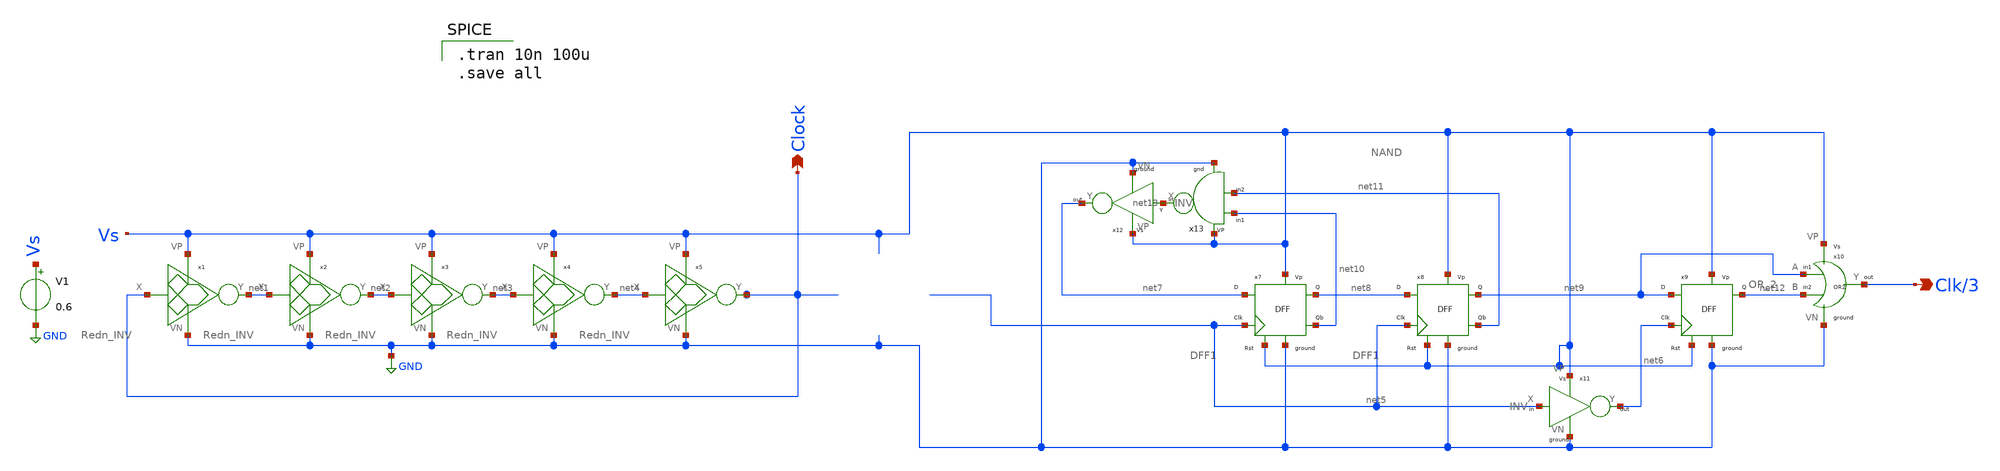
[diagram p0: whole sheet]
** sch_path: Blocks/Clk_generator/RingOsci_Div3.sch
**.subckt RingOsci_Div3 Clock Clk/3
*.opin Clock
*.opin Clk/3
V1 Vs GND 0.6
x7 net7 net5 Vs GND Vs net8 net10 DFF1
x8 net8 net5 Vs GND Vs net9 net11 DFF1
x9 net9 net6 Vs GND Vs net12 DFF
x10 net12 net9 Clk/3 Vs GND OR_2
x11 net5 net6 Vs GND INV
x12 net13 net7 Vs GND INV
x13 net11 net10 net13 Vs GND NAND
x1 Clock net1 Vs GND Redn_INV
x2 net1 net2 Vs GND Redn_INV
x3 net2 net3 Vs GND Redn_INV
x4 net3 net4 Vs GND Redn_INV
x5 net4 Clock Vs GND Redn_INV
**** begin user architecture code

.tran 10n 100u
.save all


** opencircuitdesign pdks install
.lib $::SKYWATER_MODELS/sky130.lib.spice tt


**** end user architecture code
**.ends

* expanding   symbol:  Pico_project/FlipFlops/DFF1.sym # of pins=7
** sym_path: component/FlipFlops/DFF1.sym
** sch_path: component/FlipFlops/DFF1.sch
.subckt DFF1 D Clk RST VN VP Q Qb
*.opin Q
*.iopin VN
*.iopin VP
*.ipin Clk
*.ipin D
*.ipin RST
*.opin Qb
x7 net2 net4 net3 VP VN NAND
x8 net3 Clk RST VP VN net2 NAND3
x6 Q net1 RST VP VN Qb NAND3
x4 net2 Clk net4 VP VN net1 NAND3
x5 net1 D RST VP VN net4 NAND3
x1 Qb net2 Q VP VN NAND
.ends


* expanding   symbol:  Pico_project/FlipFlops/DFF.sym # of pins=6
** sym_path: component/FlipFlops/DFF.sym
** sch_path: component/FlipFlops/DFF.sch
.subckt DFF D Clk RST VN VP Q
*.opin Q
*.iopin VN
*.iopin VP
*.ipin Clk
*.ipin D
*.ipin RST
x1 net2 net5 net4 VP VN NAND
x7 net4 Clk RST VP VN net2 NAND3
x3 Q net1 RST VP VN net3 NAND3
x4 net2 Clk net5 VP VN net1 NAND3
x5 net1 D RST VP VN net5 NAND3
x6 net3 net2 Q VP VN NAND
.ends


* expanding   symbol:  Pico_project/OR2/OR_2.sym # of pins=5
** sym_path: component/OR2/OR_2.sym
** sch_path: component/OR2/OR_2.sch
.subckt OR_2 B A Y VP VN
*.iopin VP
*.iopin VN
*.ipin A
*.ipin B
*.opin Y
XM1 net1 B VN VN sky130_fd_pr__nfet_01v8 L=0.15 W=0.42 nf=1 ad='int((nf+1)/2) * W/nf * 0.29' as='int((nf+2)/2) * W/nf * 0.29'
+ pd='2*int((nf+1)/2) * (W/nf + 0.29)' ps='2*int((nf+2)/2) * (W/nf + 0.29)' nrd='0.29 / W' nrs='0.29 / W'
+ sa=0 sb=0 sd=0 mult=1 m=1
XM2 net1 A VN VN sky130_fd_pr__nfet_01v8 L=0.15 W=0.42 nf=1 ad='int((nf+1)/2) * W/nf * 0.29' as='int((nf+2)/2) * W/nf * 0.29'
+ pd='2*int((nf+1)/2) * (W/nf + 0.29)' ps='2*int((nf+2)/2) * (W/nf + 0.29)' nrd='0.29 / W' nrs='0.29 / W'
+ sa=0 sb=0 sd=0 mult=1 m=1
XM3 net1 B net2 VP sky130_fd_pr__pfet_01v8 L=0.15 W=2.52 nf=1 ad='int((nf+1)/2) * W/nf * 0.29' as='int((nf+2)/2) * W/nf * 0.29'
+ pd='2*int((nf+1)/2) * (W/nf + 0.29)' ps='2*int((nf+2)/2) * (W/nf + 0.29)' nrd='0.29 / W' nrs='0.29 / W'
+ sa=0 sb=0 sd=0 mult=1 m=1
XM4 net2 A VP VP sky130_fd_pr__pfet_01v8 L=0.15 W=2.52 nf=1 ad='int((nf+1)/2) * W/nf * 0.29' as='int((nf+2)/2) * W/nf * 0.29'
+ pd='2*int((nf+1)/2) * (W/nf + 0.29)' ps='2*int((nf+2)/2) * (W/nf + 0.29)' nrd='0.29 / W' nrs='0.29 / W'
+ sa=0 sb=0 sd=0 mult=1 m=1
x1 net1 Y VP VN INV
.ends


* expanding   symbol:  Pico_project/INV/INV.sym # of pins=4
** sym_path: component/INV/INV.sym
** sch_path: component/INV/INV.sch
.subckt INV X Y VP VN
*.ipin X
*.opin Y
*.iopin VN
*.iopin VP
XM1 Y X VN VN sky130_fd_pr__nfet_01v8 L=0.15 W=0.42 nf=1 ad='int((nf+1)/2) * W/nf * 0.29' as='int((nf+2)/2) * W/nf * 0.29'
+ pd='2*int((nf+1)/2) * (W/nf + 0.29)' ps='2*int((nf+2)/2) * (W/nf + 0.29)' nrd='0.29 / W' nrs='0.29 / W'
+ sa=0 sb=0 sd=0 mult=1 m=1
XM2 Y X VP VP sky130_fd_pr__pfet_01v8 L=0.15 W=1.26 nf=1 ad='int((nf+1)/2) * W/nf * 0.29' as='int((nf+2)/2) * W/nf * 0.29'
+ pd='2*int((nf+1)/2) * (W/nf + 0.29)' ps='2*int((nf+2)/2) * (W/nf + 0.29)' nrd='0.29 / W' nrs='0.29 / W'
+ sa=0 sb=0 sd=0 mult=1 m=1
.ends


* expanding   symbol:  Pico_project/NAND2/NAND.sym # of pins=5
** sym_path: component/NAND2/NAND.sym
** sch_path: component/NAND2/NAND.sch
.subckt NAND B A Y VP VN
*.iopin VP
*.ipin A
*.ipin B
*.opin Y
*.iopin VN
XM1 Y A VP VP sky130_fd_pr__pfet_01v8 L=0.15 W=1.26 nf=1 ad='int((nf+1)/2) * W/nf * 0.29' as='int((nf+2)/2) * W/nf * 0.29'
+ pd='2*int((nf+1)/2) * (W/nf + 0.29)' ps='2*int((nf+2)/2) * (W/nf + 0.29)' nrd='0.29 / W' nrs='0.29 / W'
+ sa=0 sb=0 sd=0 mult=1 m=1
XM2 Y B VP VP sky130_fd_pr__pfet_01v8 L=0.15 W=1.26 nf=1 ad='int((nf+1)/2) * W/nf * 0.29' as='int((nf+2)/2) * W/nf * 0.29'
+ pd='2*int((nf+1)/2) * (W/nf + 0.29)' ps='2*int((nf+2)/2) * (W/nf + 0.29)' nrd='0.29 / W' nrs='0.29 / W'
+ sa=0 sb=0 sd=0 mult=1 m=1
XM3 Y A net1 net1 sky130_fd_pr__nfet_01v8 L=0.15 W=0.84 nf=1 ad='int((nf+1)/2) * W/nf * 0.29' as='int((nf+2)/2) * W/nf * 0.29'
+ pd='2*int((nf+1)/2) * (W/nf + 0.29)' ps='2*int((nf+2)/2) * (W/nf + 0.29)' nrd='0.29 / W' nrs='0.29 / W'
+ sa=0 sb=0 sd=0 mult=1 m=1
XM4 net1 B VN VN sky130_fd_pr__nfet_01v8 L=0.15 W=0.84 nf=1 ad='int((nf+1)/2) * W/nf * 0.29' as='int((nf+2)/2) * W/nf * 0.29'
+ pd='2*int((nf+1)/2) * (W/nf + 0.29)' ps='2*int((nf+2)/2) * (W/nf + 0.29)' nrd='0.29 / W' nrs='0.29 / W'
+ sa=0 sb=0 sd=0 mult=1 m=1
.ends


* expanding   symbol:  pico/akshat_comp/ezyzip/PICO/project_file/Redn_INV.sym # of pins=4
** sym_path: component/Reduntant_Inverter/Redn_INV.sym
** sch_path: component/Reduntant_Inverter/Redn_INV.sch
.subckt Redn_INV X Y VP VN
*.opin Y
*.ipin X
*.iopin VP
*.iopin VN
XM15 net4 X VN VN sky130_fd_pr__nfet_01v8_lvt L=0.15 W=1 nf=1 ad='int((nf+1)/2) * W/nf * 0.29' as='int((nf+2)/2) * W/nf * 0.29'
+ pd='2*int((nf+1)/2) * (W/nf + 0.29)' ps='2*int((nf+2)/2) * (W/nf + 0.29)' nrd='0.29 / W' nrs='0.29 / W'
+ sa=0 sb=0 sd=0 mult=1 m=1
XM1 net5 X net3 VN sky130_fd_pr__nfet_01v8_lvt L=0.15 W=3.25 nf=1 ad='int((nf+1)/2) * W/nf * 0.29' as='int((nf+2)/2) * W/nf * 0.29'
+ pd='2*int((nf+1)/2) * (W/nf + 0.29)' ps='2*int((nf+2)/2) * (W/nf + 0.29)' nrd='0.29 / W' nrs='0.29 / W'
+ sa=0 sb=0 sd=0 mult=1 m=1
XM16 Y X net6 VN sky130_fd_pr__nfet_01v8_lvt L=0.15 W=6.5 nf=1 ad='int((nf+1)/2) * W/nf * 0.29' as='int((nf+2)/2) * W/nf * 0.29'
+ pd='2*int((nf+1)/2) * (W/nf + 0.29)' ps='2*int((nf+2)/2) * (W/nf + 0.29)' nrd='0.29 / W' nrs='0.29 / W'
+ sa=0 sb=0 sd=0 mult=1 m=1
XM17 net3 X VN VN sky130_fd_pr__nfet_01v8_lvt L=0.15 W=3.25 nf=1 ad='int((nf+1)/2) * W/nf * 0.29' as='int((nf+2)/2) * W/nf * 0.29'
+ pd='2*int((nf+1)/2) * (W/nf + 0.29)' ps='2*int((nf+2)/2) * (W/nf + 0.29)' nrd='0.29 / W' nrs='0.29 / W'
+ sa=0 sb=0 sd=0 mult=1 m=1
XM18 net2 X VN VN sky130_fd_pr__nfet_01v8_lvt L=0.15 W=1.5 nf=1 ad='int((nf+1)/2) * W/nf * 0.29' as='int((nf+2)/2) * W/nf * 0.29'
+ pd='2*int((nf+1)/2) * (W/nf + 0.29)' ps='2*int((nf+2)/2) * (W/nf + 0.29)' nrd='0.29 / W' nrs='0.29 / W'
+ sa=0 sb=0 sd=0 mult=1 m=1
XM19 net1 X VN VN sky130_fd_pr__nfet_01v8_lvt L=0.15 W=6.5 nf=1 ad='int((nf+1)/2) * W/nf * 0.29' as='int((nf+2)/2) * W/nf * 0.29'
+ pd='2*int((nf+1)/2) * (W/nf + 0.29)' ps='2*int((nf+2)/2) * (W/nf + 0.29)' nrd='0.29 / W' nrs='0.29 / W'
+ sa=0 sb=0 sd=0 mult=1 m=1
XM20 net6 X net1 VN sky130_fd_pr__nfet_01v8_lvt L=0.15 W=6.5 nf=1 ad='int((nf+1)/2) * W/nf * 0.29' as='int((nf+2)/2) * W/nf * 0.29'
+ pd='2*int((nf+1)/2) * (W/nf + 0.29)' ps='2*int((nf+2)/2) * (W/nf + 0.29)' nrd='0.29 / W' nrs='0.29 / W'
+ sa=0 sb=0 sd=0 mult=1 m=1
XM2 net4 X VP VP sky130_fd_pr__pfet_01v8 L=0.15 W=10 nf=1 ad='int((nf+1)/2) * W/nf * 0.29' as='int((nf+2)/2) * W/nf * 0.29'
+ pd='2*int((nf+1)/2) * (W/nf + 0.29)' ps='2*int((nf+2)/2) * (W/nf + 0.29)' nrd='0.29 / W' nrs='0.29 / W'
+ sa=0 sb=0 sd=0 mult=1 m=1
XM5 net5 X net4 net4 sky130_fd_pr__pfet_01v8 L=0.15 W=10 nf=1 ad='int((nf+1)/2) * W/nf * 0.29' as='int((nf+2)/2) * W/nf * 0.29'
+ pd='2*int((nf+1)/2) * (W/nf + 0.29)' ps='2*int((nf+2)/2) * (W/nf + 0.29)' nrd='0.29 / W' nrs='0.29 / W'
+ sa=0 sb=0 sd=0 mult=1 m=1
XM6 Y X net5 VP sky130_fd_pr__pfet_01v8 L=0.15 W=10 nf=1 ad='int((nf+1)/2) * W/nf * 0.29' as='int((nf+2)/2) * W/nf * 0.29'
+ pd='2*int((nf+1)/2) * (W/nf + 0.29)' ps='2*int((nf+2)/2) * (W/nf + 0.29)' nrd='0.29 / W' nrs='0.29 / W'
+ sa=0 sb=0 sd=0 mult=1 m=1
XM8 net3 X VP VP sky130_fd_pr__pfet_01v8 L=0.15 W=2 nf=1 ad='int((nf+1)/2) * W/nf * 0.29' as='int((nf+2)/2) * W/nf * 0.29'
+ pd='2*int((nf+1)/2) * (W/nf + 0.29)' ps='2*int((nf+2)/2) * (W/nf + 0.29)' nrd='0.29 / W' nrs='0.29 / W'
+ sa=0 sb=0 sd=0 mult=1 m=1
XM12 net2 X VP VP sky130_fd_pr__pfet_01v8 L=0.15 W=5 nf=1 ad='int((nf+1)/2) * W/nf * 0.29' as='int((nf+2)/2) * W/nf * 0.29'
+ pd='2*int((nf+1)/2) * (W/nf + 0.29)' ps='2*int((nf+2)/2) * (W/nf + 0.29)' nrd='0.29 / W' nrs='0.29 / W'
+ sa=0 sb=0 sd=0 mult=1 m=1
XM14 net6 X net2 VP sky130_fd_pr__pfet_01v8 L=0.15 W=5 nf=1 ad='int((nf+1)/2) * W/nf * 0.29' as='int((nf+2)/2) * W/nf * 0.29'
+ pd='2*int((nf+1)/2) * (W/nf + 0.29)' ps='2*int((nf+2)/2) * (W/nf + 0.29)' nrd='0.29 / W' nrs='0.29 / W'
+ sa=0 sb=0 sd=0 mult=1 m=1
XM21 net1 X VP VP sky130_fd_pr__pfet_01v8 L=0.15 W=1.5 nf=1 ad='int((nf+1)/2) * W/nf * 0.29' as='int((nf+2)/2) * W/nf * 0.29'
+ pd='2*int((nf+1)/2) * (W/nf + 0.29)' ps='2*int((nf+2)/2) * (W/nf + 0.29)' nrd='0.29 / W' nrs='0.29 / W'
+ sa=0 sb=0 sd=0 mult=1 m=1
.ends


* expanding   symbol:  component/NAND3/NAND3.sym # of pins=6
** sym_path: component/NAND3/NAND3.sym
** sch_path: component/NAND3/NAND3.sch
.subckt NAND3 A B C VP VN Y
*.iopin VP
*.iopin VN
*.ipin A
*.ipin B
*.ipin C
*.opin Y
XM1 Y A net1 VN sky130_fd_pr__nfet_01v8 L=0.15 W=1.26 nf=1 ad='int((nf+1)/2) * W/nf * 0.29' as='int((nf+2)/2) * W/nf * 0.29'
+ pd='2*int((nf+1)/2) * (W/nf + 0.29)' ps='2*int((nf+2)/2) * (W/nf + 0.29)' nrd='0.29 / W' nrs='0.29 / W'
+ sa=0 sb=0 sd=0 mult=1 m=1
XM2 net1 B net2 VN sky130_fd_pr__nfet_01v8 L=0.15 W=1.26 nf=1 ad='int((nf+1)/2) * W/nf * 0.29' as='int((nf+2)/2) * W/nf * 0.29'
+ pd='2*int((nf+1)/2) * (W/nf + 0.29)' ps='2*int((nf+2)/2) * (W/nf + 0.29)' nrd='0.29 / W' nrs='0.29 / W'
+ sa=0 sb=0 sd=0 mult=1 m=1
XM3 net2 C VN VN sky130_fd_pr__nfet_01v8 L=0.15 W=1.26 nf=1 ad='int((nf+1)/2) * W/nf * 0.29' as='int((nf+2)/2) * W/nf * 0.29'
+ pd='2*int((nf+1)/2) * (W/nf + 0.29)' ps='2*int((nf+2)/2) * (W/nf + 0.29)' nrd='0.29 / W' nrs='0.29 / W'
+ sa=0 sb=0 sd=0 mult=1 m=1
XM4 Y A VP VP sky130_fd_pr__pfet_01v8 L=0.15 W=1.26 nf=1 ad='int((nf+1)/2) * W/nf * 0.29' as='int((nf+2)/2) * W/nf * 0.29'
+ pd='2*int((nf+1)/2) * (W/nf + 0.29)' ps='2*int((nf+2)/2) * (W/nf + 0.29)' nrd='0.29 / W' nrs='0.29 / W'
+ sa=0 sb=0 sd=0 mult=1 m=1
XM5 Y B VP VP sky130_fd_pr__pfet_01v8 L=0.15 W=1.26 nf=1 ad='int((nf+1)/2) * W/nf * 0.29' as='int((nf+2)/2) * W/nf * 0.29'
+ pd='2*int((nf+1)/2) * (W/nf + 0.29)' ps='2*int((nf+2)/2) * (W/nf + 0.29)' nrd='0.29 / W' nrs='0.29 / W'
+ sa=0 sb=0 sd=0 mult=1 m=1
XM6 Y C VP VP sky130_fd_pr__pfet_01v8 L=0.15 W=1.26 nf=1 ad='int((nf+1)/2) * W/nf * 0.29' as='int((nf+2)/2) * W/nf * 0.29'
+ pd='2*int((nf+1)/2) * (W/nf + 0.29)' ps='2*int((nf+2)/2) * (W/nf + 0.29)' nrd='0.29 / W' nrs='0.29 / W'
+ sa=0 sb=0 sd=0 mult=1 m=1
.ends

.GLOBAL GND
.end
